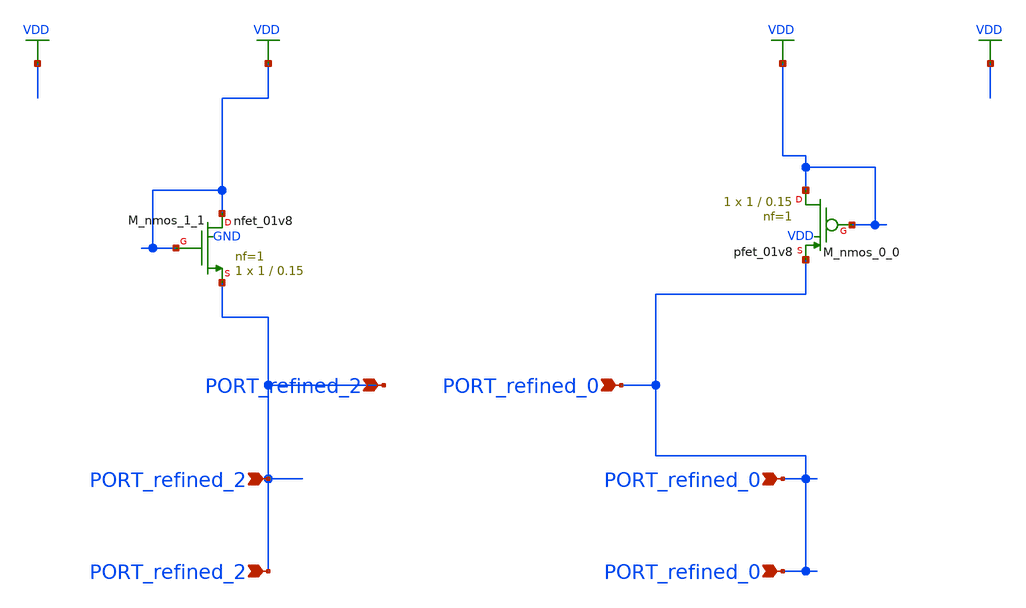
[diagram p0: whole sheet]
** sch_path: schematics/AMSNet/807.sch
**.subckt 807 PORT_refined_2 PORT_refined_2 PORT_refined_2 PORT_refined_0 PORT_refined_0
*+ PORT_refined_0
*.ipin PORT_refined_2
*.ipin PORT_refined_2
*.ipin PORT_refined_2
*.ipin PORT_refined_0
*.ipin PORT_refined_0
*.ipin PORT_refined_0
XM_nmos_0_0 VDD VDD PORT_refined_0 VDD sky130_fd_pr__pfet_01v8 L=0.15 W=1 nf=1 ad='int((1 + 1)/2) * 1 / 1 * 0.29'
+ as='int((1 + 2)/2) * 1 / 1 * 0.29' pd='2*int((1 + 1)/2) * (1 / 1 + 0.29)' ps='2*int((1 + 2)/2) * (1 / 1 + 0.29)'
+ nrd='0.29 / 1 ' nrs='0.29 / 1 ' sa=0 sb=0 sd=0 mult=1 m=1
XM_nmos_1_1 VDD VDD PORT_refined_2 GND sky130_fd_pr__nfet_01v8 L=0.15 W=1 nf=1 ad='int((1 + 1)/2) * 1 / 1 * 0.29'
+ as='int((1 + 2)/2) * 1 / 1 * 0.29' pd='2*int((1 + 1)/2) * (1 / 1 + 0.29)' ps='2*int((1 + 2)/2) * (1 / 1 + 0.29)'
+ nrd='0.29 / 1 ' nrs='0.29 / 1 ' sa=0 sb=0 sd=0 mult=1 m=1
**.ends
.GLOBAL VDD
.end
